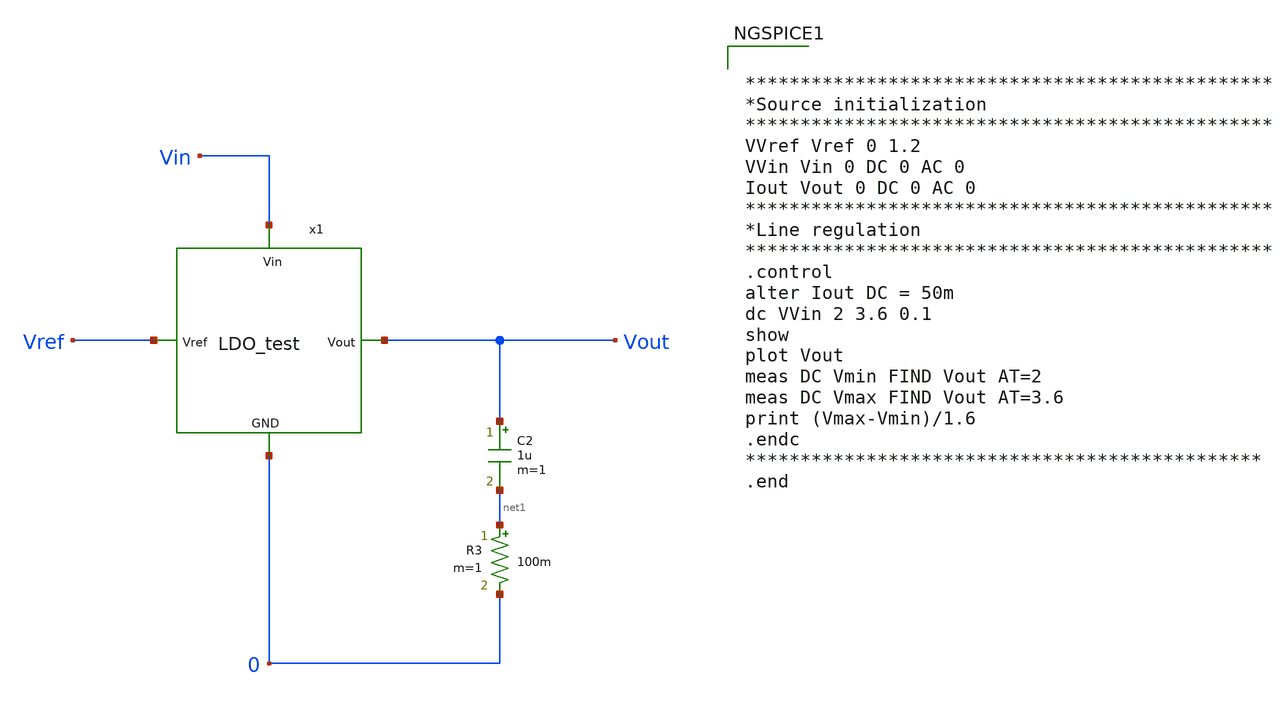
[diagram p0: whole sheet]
** sch_path: Analog_Blocks/LDO/Testbench/LDO_test_TB.sch
**.subckt LDO_test_TB
C2 Vout net1 1u m=1
R3 net1 0 100m m=1
x1 Vin Vref Vout 0 LDO_test
**** begin user architecture code


************************************************
*Source initialization
************************************************
VVref Vref 0 1.2
VVin Vin 0 DC 0 AC 0
Iout Vout 0 DC 0 AC 0
************************************************
*Line regulation
************************************************
.control
alter Iout DC = 50m
dc VVin 2 3.6 0.1
show
plot Vout
meas DC Vmin FIND Vout AT=2
meas DC Vmax FIND Vout AT=3.6
print (Vmax-Vmin)/1.6
.endc
***********************************************
.end




.param mc_mm_switch=0
.param mc_pr_switch=0
.include ~/mabrains/pdks/sky130A/libs.ref/sky130_fd_pr/spice/sky130_fd_pr__nfet_01v8__tt.corner.spice
.include ~/mabrains/pdks/sky130A/libs.ref/sky130_fd_pr/spice/sky130_fd_pr__nfet_01v8_lvt__tt.corner.spice
.include ~/mabrains/pdks/sky130A/libs.ref/sky130_fd_pr/spice/sky130_fd_pr__pfet_01v8__tt.corner.spice
.include ~/mabrains/pdks/sky130A/libs.ref/sky130_fd_pr/spice/sky130_fd_pr__nfet_03v3_nvt__tt.corner.spice
.include ~/mabrains/pdks/sky130A/libs.ref/sky130_fd_pr/spice/sky130_fd_pr__nfet_05v0_nvt__tt.corner.spice
.include ~/mabrains/pdks/sky130A/libs.ref/sky130_fd_pr/spice/sky130_fd_pr__esd_nfet_01v8__tt.corner.spice
.include ~/mabrains/pdks/sky130A/libs.ref/sky130_fd_pr/spice/sky130_fd_pr__pfet_01v8_lvt__tt.corner.spice
.include ~/mabrains/pdks/sky130A/libs.ref/sky130_fd_pr/spice/sky130_fd_pr__pfet_01v8_hvt__tt.corner.spice
.include ~/mabrains/pdks/sky130A/libs.ref/sky130_fd_pr/spice/sky130_fd_pr__esd_pfet_g5v0d10v5__tt.corner.spice
.include ~/mabrains/pdks/sky130A/libs.ref/sky130_fd_pr/spice/sky130_fd_pr__pfet_g5v0d10v5__tt.corner.spice
.include ~/mabrains/pdks/sky130A/libs.ref/sky130_fd_pr/spice/sky130_fd_pr__pfet_g5v0d16v0__tt.corner.spice
.include ~/mabrains/pdks/sky130A/libs.ref/sky130_fd_pr/spice/sky130_fd_pr__nfet_g5v0d10v5__tt.corner.spice
.include ~/mabrains/pdks/sky130A/libs.ref/sky130_fd_pr/spice/sky130_fd_pr__nfet_g5v0d16v0__tt_discrete.corner.spice
.include ~/mabrains/pdks/sky130A/libs.ref/sky130_fd_pr/spice/sky130_fd_pr__esd_nfet_g5v0d10v5__tt.corner.spice
.include ~/mabrains/pdks/sky130A/libs.tech/ngspice/corners/tt/nonfet.spice
* Mismatch parameters
.include ~/mabrains/pdks/sky130A/libs.ref/sky130_fd_pr/spice/sky130_fd_pr__nfet_01v8__mismatch.corner.spice
.include ~/mabrains/pdks/sky130A/libs.ref/sky130_fd_pr/spice/sky130_fd_pr__pfet_01v8__mismatch.corner.spice
.include ~/mabrains/pdks/sky130A/libs.ref/sky130_fd_pr/spice/sky130_fd_pr__nfet_01v8_lvt__mismatch.corner.spice
.include ~/mabrains/pdks/sky130A/libs.ref/sky130_fd_pr/spice/sky130_fd_pr__pfet_01v8_lvt__mismatch.corner.spice
.include ~/mabrains/pdks/sky130A/libs.ref/sky130_fd_pr/spice/sky130_fd_pr__pfet_01v8_hvt__mismatch.corner.spice
.include ~/mabrains/pdks/sky130A/libs.ref/sky130_fd_pr/spice/sky130_fd_pr__nfet_g5v0d10v5__mismatch.corner.spice
.include ~/mabrains/pdks/sky130A/libs.ref/sky130_fd_pr/spice/sky130_fd_pr__pfet_g5v0d10v5__mismatch.corner.spice
.include ~/mabrains/pdks/sky130A/libs.ref/sky130_fd_pr/spice/sky130_fd_pr__nfet_05v0_nvt__mismatch.corner.spice
.include ~/mabrains/pdks/sky130A/libs.ref/sky130_fd_pr/spice/sky130_fd_pr__nfet_03v3_nvt__mismatch.corner.spice
* Resistor/Capacitor
.include ~/mabrains/pdks/sky130A/libs.tech/ngspice/r+c/res_typical__cap_typical.spice
.include ~/mabrains/pdks/sky130A/libs.tech/ngspice/r+c/res_typical__cap_typical__lin.spice
* Special cells
.include ~/mabrains/pdks/sky130A/libs.tech/ngspice/corners/tt/specialized_cells.spice
* All models
.include ~/mabrains/pdks/sky130A/libs.tech/ngspice/all.spice
* Corner
.include ~/mabrains/pdks/sky130A/libs.tech/ngspice/corners/tt/rf.spice



**** end user architecture code
**.ends
.end
